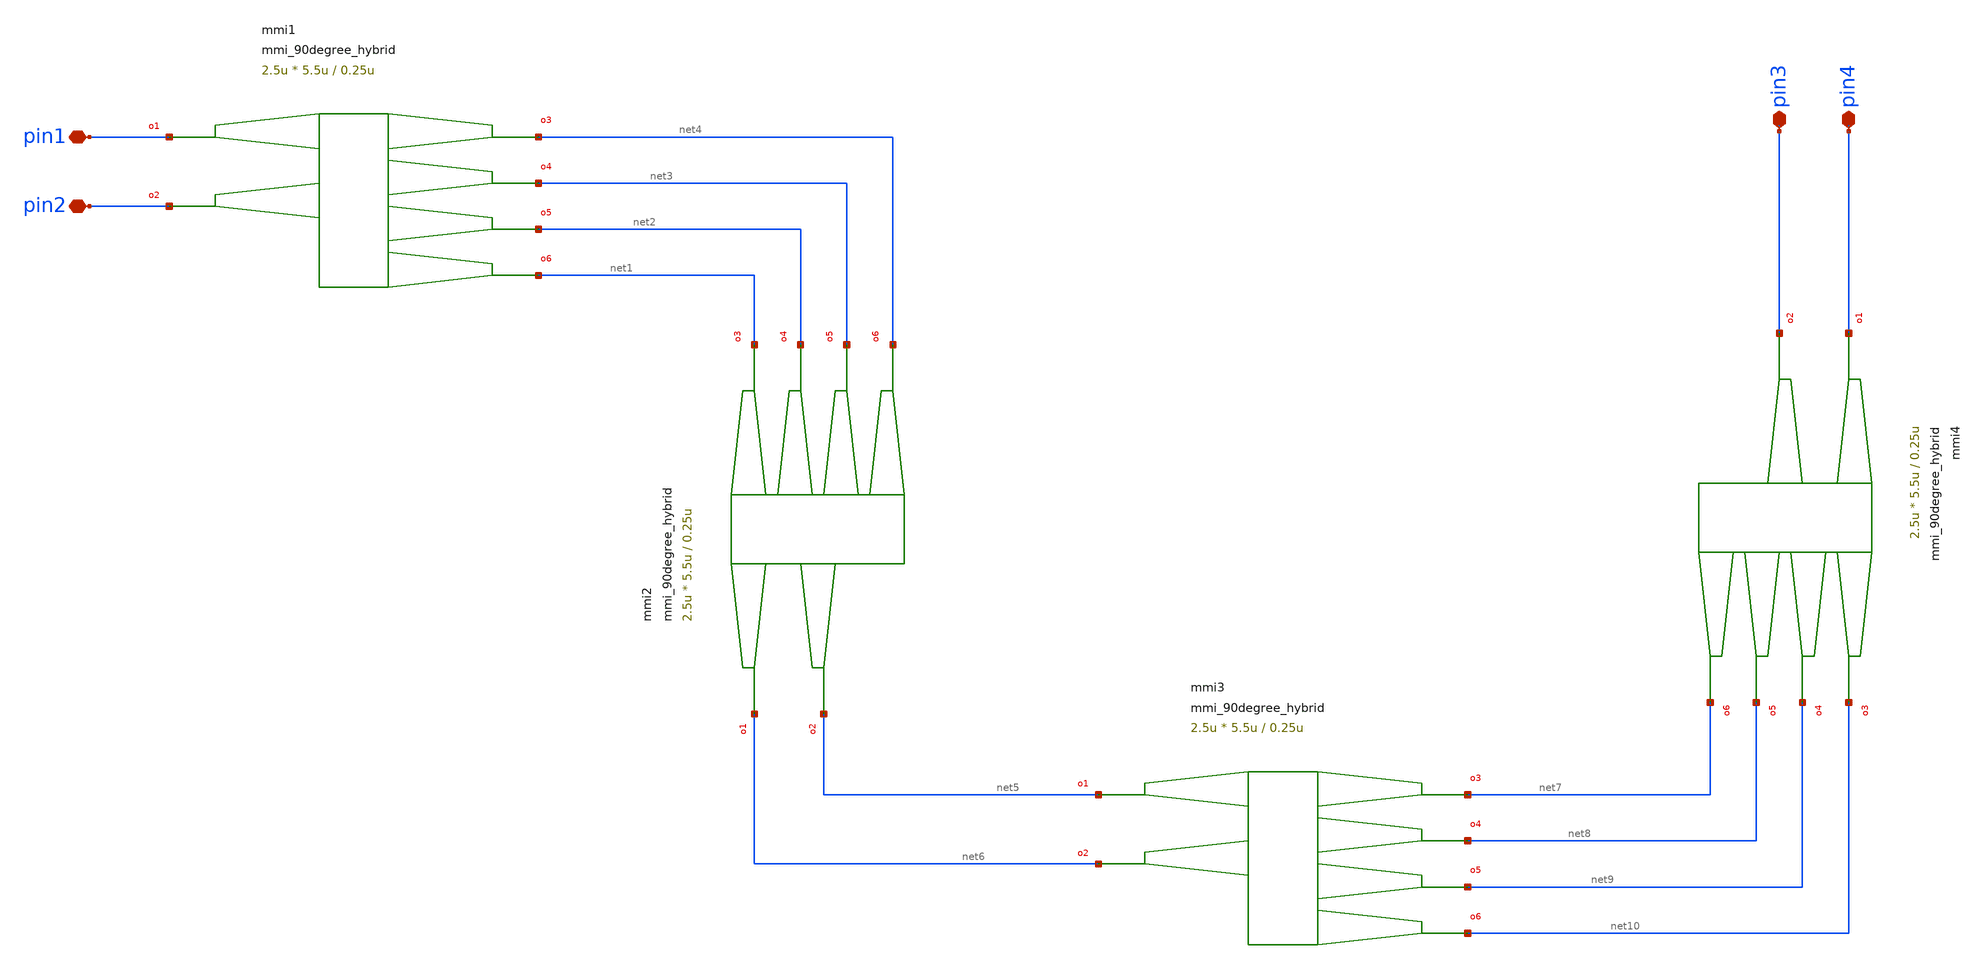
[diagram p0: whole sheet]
** sch_path: xschem/tests/test_sch/test_mmi_90degree_hybrid.sch
* Copyright (c) 2024, Mabrains LLC
* Licensed under the GNU Lesser General Public License, Version 3.0 (the "License");
* you may not use this file except in compliance with the License.
* GNU Lesser General Public License
* Version 3, 29 June 2007
* This program is free software: you can redistribute it and/or modify
* it under the terms of the GNU Lesser General Public License as published
* by the Free Software Foundation, either version 3 of the License, or
* (at your option) any later version.
* This program is distributed in the hope that it will be useful,
* but WITHOUT ANY WARRANTY; without even the implied warranty of
* MERCHANTABILITY or FITNESS FOR A PARTICULAR PURPOSE.  See the
* GNU Lesser General Public License for more details.
* You should have received a copy of the GNU Lesser General Public License
* along with this program.  If not, see <https://www.gnu.org/licenses/>.
* SPDX-License-Identifier: LGPL-3.0
**.subckt test_mmi_90degree_hybrid pin3 pin4 pin1 pin2
*.iopin pin3
*.iopin pin4
*.iopin pin1
*.iopin pin2
Pmmi1 pin1 pin2 net4 net3 net2 net1 mmi_90degree_hybrid width=0.5u width_taper=1u length_taper=10u
+ length_mmi=5.5u width_mmi=2.5u gap_mmi=0.25u
Pmmi2 net6 net5 net1 net2 net3 net4 mmi_90degree_hybrid width=0.5u width_taper=1u length_taper=10u
+ length_mmi=5.5u width_mmi=2.5u gap_mmi=0.25u
Pmmi3 net5 net6 net7 net8 net9 net10 mmi_90degree_hybrid width=0.5u width_taper=1u length_taper=10u
+ length_mmi=5.5u width_mmi=2.5u gap_mmi=0.25u
Pmmi4 pin4 pin3 net10 net9 net8 net7 mmi_90degree_hybrid width=0.5u width_taper=1u length_taper=10u
+ length_mmi=5.5u width_mmi=2.5u gap_mmi=0.25u
**.ends
.end
